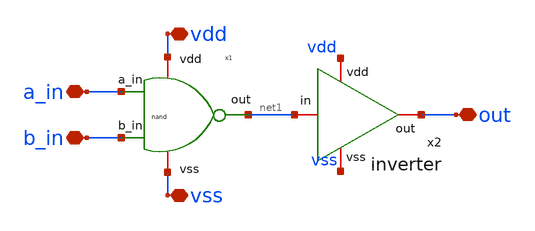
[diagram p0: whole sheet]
** sch_path: design/blocks/andgate/schematic/andgate.sch
**.subckt andgate a_in b_in out vdd vss
*.iopin a_in
*.iopin b_in
*.iopin out
*.iopin vdd
*.iopin vss
x1 vdd a_in net1 b_in vss nand
x2 vdd out net1 vss inverter
**.ends

* expanding   symbol:  blocks/andgate/schematic/nand.sym # of pins=5
** sym_path: design/blocks/andgate/schematic/nand.sym
** sch_path: design/blocks/andgate/schematic/nand.sch
.subckt nand vdd a_in out b_in vss
*.iopin vdd
*.iopin vss
*.ipin a_in
*.ipin b_in
*.opin out
XM1 net1 b_in vss vss sg13_lv_nmos w=0.45u l=0.13u ng=1 m=1 mm_ok=1
XM2 out a_in net1 vss sg13_lv_nmos w=0.15u l=0.13u ng=1 m=1 mm_ok=1
XM3 out b_in vdd vdd sg13_lv_pmos w=0.15u l=0.13u ng=1 m=1 mm_ok=1
XM4 out a_in vdd vdd sg13_lv_pmos w=0.15u l=0.13u ng=1 m=1 mm_ok=1
.ends


* expanding   symbol:  blocks/inverter/schematic/inverter.sym # of pins=4
** sym_path: blocks/inverter/schematic/inverter.sym
** sch_path: blocks/inverter/schematic/inverter.sch
.subckt inverter vdd out in vss
*.iopin vdd
*.iopin vss
*.iopin out
*.iopin in
XM2 out in vdd vdd sg13_lv_pmos w=0.3u l=0.13u ng=1 m=1 mm_ok=1
XM1 out in vss vss sg13_lv_nmos w=0.15u l=0.13u ng=1 m=1 mm_ok=1
.ends

.end
